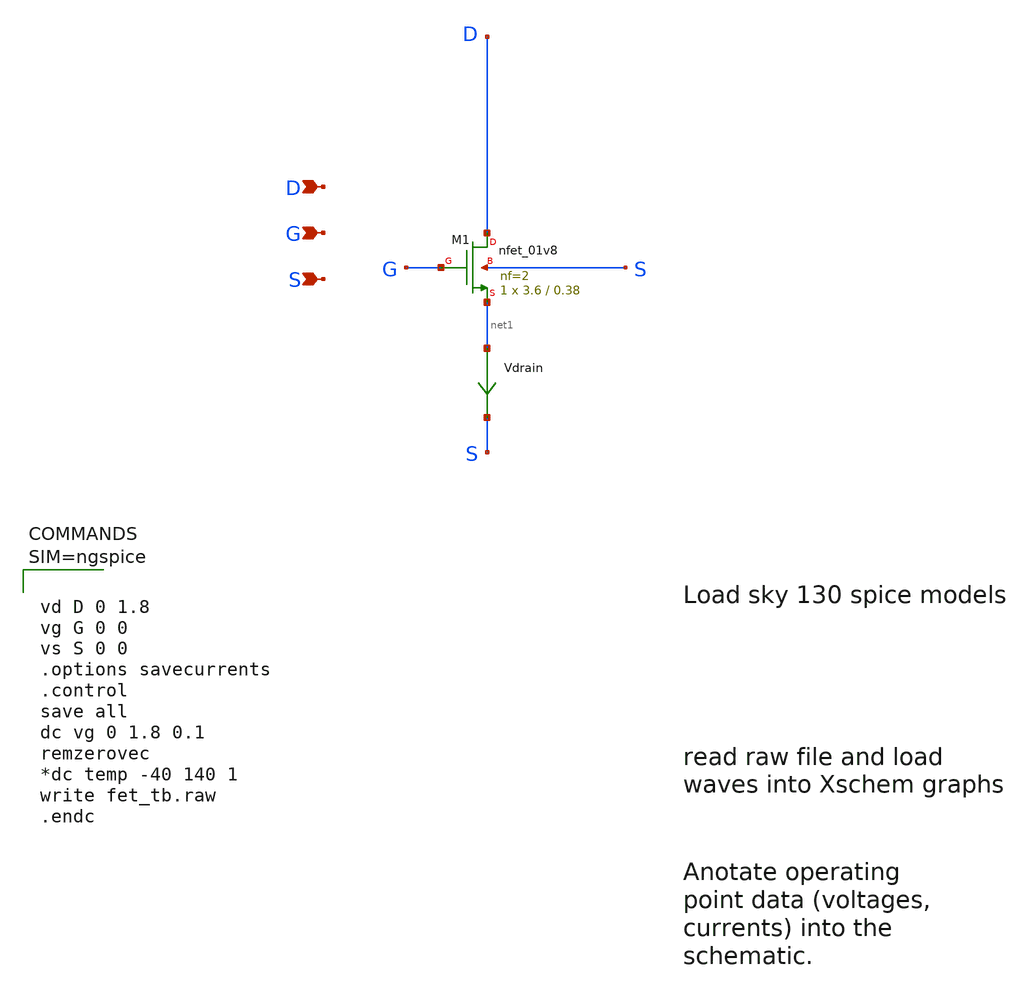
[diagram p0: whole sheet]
** sch_path: xschem/fet_tb.sch
**.subckt fet_tb D G S
*.ipin D
*.ipin G
*.ipin S
XM1 D G net1 S sky130_fd_pr__nfet_01v8 L=0.38 W=3.6 nf=2 ad='int((nf+1)/2) * W/nf * 0.29' as='int((nf+2)/2) * W/nf * 0.29'
+ pd='2*int((nf+1)/2) * (W/nf + 0.29)' ps='2*int((nf+2)/2) * (W/nf + 0.29)' nrd='0.29 / W' nrs='0.29 / W'
+ sa=0 sb=0 sd=0 mult=1 m=1
Vdrain net1 S 0
.save i(vdrain)
**** begin user architecture code

** opencircuitdesign pdks install
.lib $::SKYWATER_MODELS/sky130.lib.spice tt





vd D 0 1.8
vg G 0 0
vs S 0 0
.options savecurrents
.control
save all
dc vg 0 1.8 0.1
remzerovec
*dc temp -40 140 1
write fet_tb.raw
.endc




**** end user architecture code
**.ends
.end
